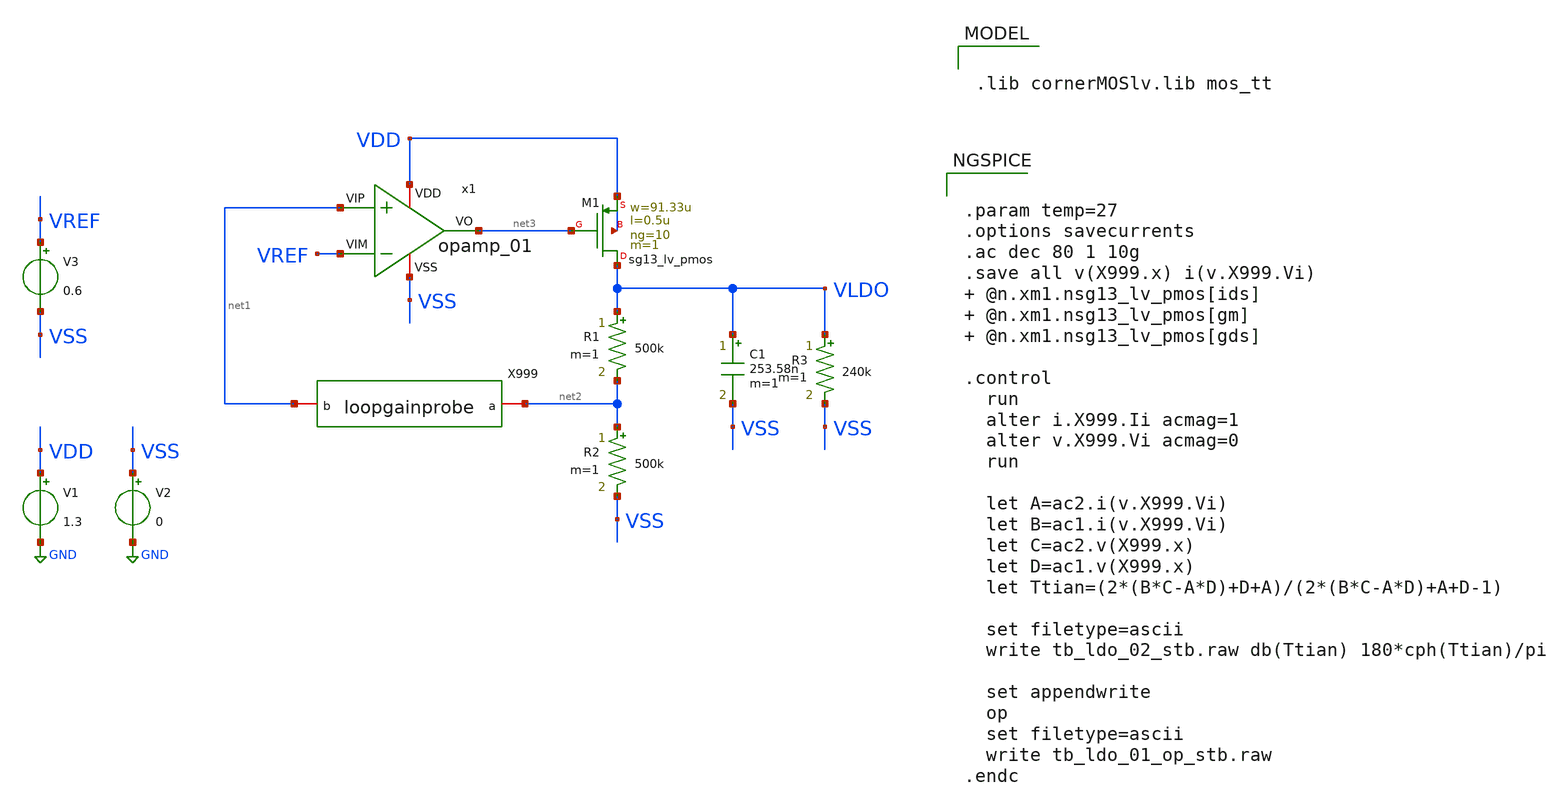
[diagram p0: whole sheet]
** sch_path: analog/tb/tb_ldo_01_stb.sch
**.subckt tb_ldo_01_stb
C1 VLDO VSS 253.58n m=1
V1 VDD GND 1.3
V2 VSS GND 0
V3 VREF VSS 0.6
x1 VDD net1 net3 VSS VREF opamp_01
XM1 VLDO net3 VDD VDD sg13_lv_pmos w=91.33u l=0.5u ng=10 m=1 mm_ok=1
R2 net2 VSS 500k m=1
R1 VLDO net2 500k m=1
R3 VLDO VSS 240k m=1
X999 net1 net2 loopgainprobe
**** begin user architecture code


.param temp=27
.options savecurrents
.ac dec 80 1 10g
.save all v(X999.x) i(v.X999.Vi)  @n.xm1.nsg13_lv_pmos[ids]  @n.xm1.nsg13_lv_pmos[gm]  @n.xm1.nsg13_lv_pmos[gds]

.control
  run
  alter i.X999.Ii acmag=1
  alter v.X999.Vi acmag=0
  run

  let A=ac2.i(v.X999.Vi)
  let B=ac1.i(v.X999.Vi)
  let C=ac2.v(X999.x)
  let D=ac1.v(X999.x)
  let Ttian=(2*(B*C-A*D)+D+A)/(2*(B*C-A*D)+A+D-1)

  set filetype=ascii
  write tb_ldo_02_stb.raw db(Ttian) 180*cph(Ttian)/pi

  set appendwrite
  op
  set filetype=ascii
  write tb_ldo_01_op_stb.raw
.endc




.lib cornerMOSlv.lib mos_tt


**** end user architecture code
**.ends

* expanding   symbol:  opamp_01.sym # of pins=5
** sym_path: analog/core/opamp_01.sym
** sch_path: analog/core/opamp_01.sch
.subckt opamp_01 VDD VIP VO VSS VIM
*.iopin VIM
*.iopin VIP
*.iopin VSS
*.iopin VDD
*.iopin VO
XM1 net2 VIP net1 VSS sg13_lv_nmos w=10u l=0.25u ng=1 m=1 mm_ok=1
XM2 VO VIM net1 VSS sg13_lv_nmos w=10u l=0.25u ng=1 m=1 mm_ok=1
XM3 net2 net2 VDD VDD sg13_lv_pmos w=1u l=4u ng=1 m=1 mm_ok=1
XM4 VO net2 VDD VDD sg13_lv_pmos w=1u l=4u ng=1 m=1 mm_ok=1
XM5 net1 net3 VSS VSS sg13_lv_nmos w=2u l=2u ng=1 m=1 mm_ok=1
XM6 net3 net3 VSS VSS sg13_lv_nmos w=2u l=2u ng=1 m=1 mm_ok=1
I0 VDD net3 100n
.ends


* expanding   symbol:  loopgainprobe.sym # of pins=2
** sym_path: analog/tb/loopgainprobe.sym
** sch_path: analog/tb/loopgainprobe.sch
.subckt loopgainprobe b a
*.iopin a
*.iopin b
Vi x a dc 0 ac 1
Ii GND x dc 0 ac 0
Vnodebuffer b x 0
.ends

.GLOBAL GND
.end
